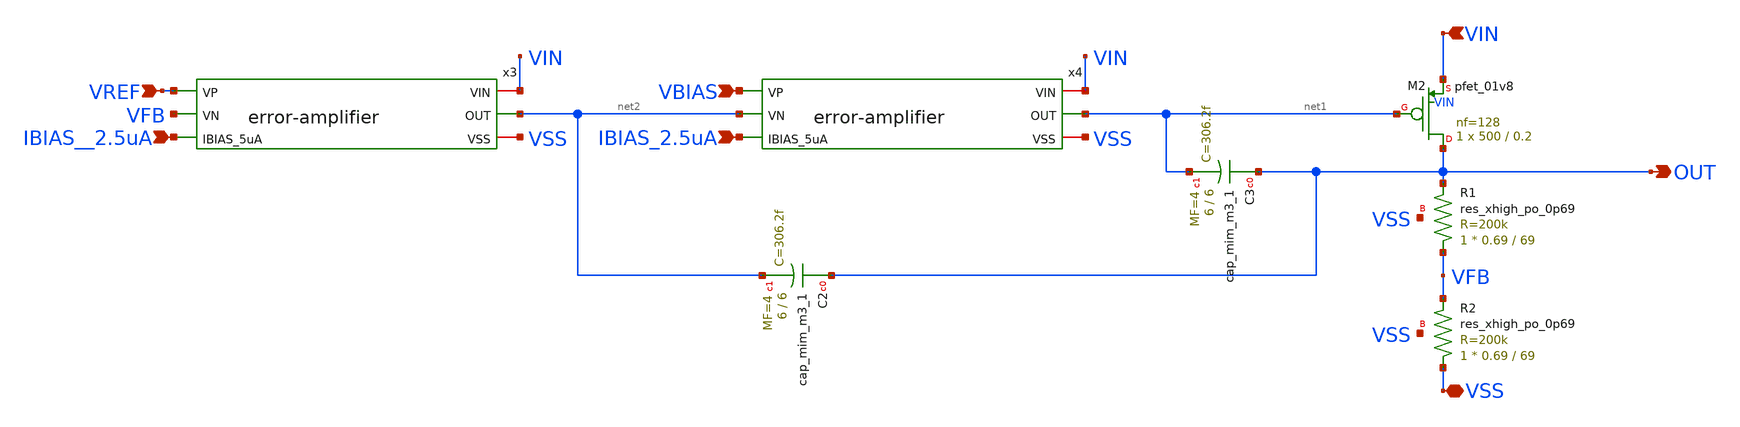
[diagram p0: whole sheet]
** sch_path: xschem/ldo_andriansyah/schematics/ldo-top.sch
**.subckt ldo-top VREF VIN IBIAS__2.5uA VSS IBIAS_2.5uA VBIAS OUT
*.ipin VREF
*.ipin VIN
*.ipin IBIAS__2.5uA
*.iopin VSS
*.ipin IBIAS_2.5uA
*.ipin VBIAS
*.opin OUT
XC2 OUT net2 sky130_fd_pr__cap_mim_m3_1 W=6 L=6 MF=4 m=4
XC3 OUT net1 sky130_fd_pr__cap_mim_m3_1 W=6 L=6 MF=4 m=4
x3 VIN VREF VFB IBIAS__2.5uA net2 VSS error-amplifier
XR1 VFB OUT VSS sky130_fd_pr__res_xhigh_po_0p69 L=69 mult=1 m=1
XR2 VSS VFB VSS sky130_fd_pr__res_xhigh_po_0p69 L=69 mult=1 m=1
XM2 OUT net1 VIN VIN sky130_fd_pr__pfet_01v8 L=0.2 W=500 nf=128 ad='int((nf+1)/2) * W/nf * 0.29' as='int((nf+2)/2) * W/nf * 0.29'
+ pd='2*int((nf+1)/2) * (W/nf + 0.29)' ps='2*int((nf+2)/2) * (W/nf + 0.29)' nrd='0.29 / W' nrs='0.29 / W'
+ sa=0 sb=0 sd=0 mult=1 m=1
x4 VIN VBIAS net2 IBIAS_2.5uA net1 VSS error-amplifier
**.ends

* expanding   symbol:
*+  /foss/designs/2026/tt_sky26b_ldo_andriansyah/xschem/error-amplifier/error-amplifier.sym # of pins=6
** sym_path: xschem/error-amplifier/error-amplifier.sym
** sch_path: xschem/error-amplifier/error-amplifier.sch
.subckt error-amplifier VIN VP VN IBIAS_5uA OUT VSS
*.ipin IBIAS_5uA
*.ipin VN
*.ipin VP
*.iopin VIN
*.iopin VSS
*.opin OUT
XM1 net2 net2 VSS VSS sky130_fd_pr__nfet_01v8 L=0.6 W=4.2 nf=4 ad='int((nf+1)/2) * W/nf * 0.29' as='int((nf+2)/2) * W/nf * 0.29'
+ pd='2*int((nf+1)/2) * (W/nf + 0.29)' ps='2*int((nf+2)/2) * (W/nf + 0.29)' nrd='0.29 / W' nrs='0.29 / W'
+ sa=0 sb=0 sd=0 mult=1 m=1
XM2 OUT net2 VSS VSS sky130_fd_pr__nfet_01v8 L=0.6 W=4.2 nf=4 ad='int((nf+1)/2) * W/nf * 0.29' as='int((nf+2)/2) * W/nf * 0.29'
+ pd='2*int((nf+1)/2) * (W/nf + 0.29)' ps='2*int((nf+2)/2) * (W/nf + 0.29)' nrd='0.29 / W' nrs='0.29 / W'
+ sa=0 sb=0 sd=0 mult=1 m=1
XM3 net2 VN net1 VDD sky130_fd_pr__pfet_01v8 L=0.6 W=28 nf=4 ad='int((nf+1)/2) * W/nf * 0.29' as='int((nf+2)/2) * W/nf * 0.29'
+ pd='2*int((nf+1)/2) * (W/nf + 0.29)' ps='2*int((nf+2)/2) * (W/nf + 0.29)' nrd='0.29 / W' nrs='0.29 / W'
+ sa=0 sb=0 sd=0 mult=1 m=1
XM4 OUT VP net1 VDD sky130_fd_pr__pfet_01v8 L=0.6 W=28 nf=4 ad='int((nf+1)/2) * W/nf * 0.29' as='int((nf+2)/2) * W/nf * 0.29'
+ pd='2*int((nf+1)/2) * (W/nf + 0.29)' ps='2*int((nf+2)/2) * (W/nf + 0.29)' nrd='0.29 / W' nrs='0.29 / W'
+ sa=0 sb=0 sd=0 mult=1 m=1
XM5 net1 IBIAS_5uA VIN VIN sky130_fd_pr__pfet_01v8 L=0.6 W=6.6 nf=4 ad='int((nf+1)/2) * W/nf * 0.29'
+ as='int((nf+2)/2) * W/nf * 0.29' pd='2*int((nf+1)/2) * (W/nf + 0.29)' ps='2*int((nf+2)/2) * (W/nf + 0.29)'
+ nrd='0.29 / W' nrs='0.29 / W' sa=0 sb=0 sd=0 mult=1 m=1
XM6 IBIAS_5uA IBIAS_5uA VIN VIN sky130_fd_pr__pfet_01v8 L=0.6 W=6.6 nf=4 ad='int((nf+1)/2) * W/nf * 0.29'
+ as='int((nf+2)/2) * W/nf * 0.29' pd='2*int((nf+1)/2) * (W/nf + 0.29)' ps='2*int((nf+2)/2) * (W/nf + 0.29)'
+ nrd='0.29 / W' nrs='0.29 / W' sa=0 sb=0 sd=0 mult=1 m=1
XM7 VDD VDD VDD VDD sky130_fd_pr__pfet_01v8 L=0.6 W=7 nf=1 ad='int((nf+1)/2) * W/nf * 0.29' as='int((nf+2)/2) * W/nf * 0.29'
+ pd='2*int((nf+1)/2) * (W/nf + 0.29)' ps='2*int((nf+2)/2) * (W/nf + 0.29)' nrd='0.29 / W' nrs='0.29 / W'
+ sa=0 sb=0 sd=0 mult=1 m=1
XM8 VSS VSS VSS VSS sky130_fd_pr__nfet_01v8 L=0.6 W=1.05 nf=1 ad='int((nf+1)/2) * W/nf * 0.29' as='int((nf+2)/2) * W/nf * 0.29'
+ pd='2*int((nf+1)/2) * (W/nf + 0.29)' ps='2*int((nf+2)/2) * (W/nf + 0.29)' nrd='0.29 / W' nrs='0.29 / W'
+ sa=0 sb=0 sd=0 mult=1 m=1
XM9 VDD VDD VDD VDD sky130_fd_pr__pfet_01v8 L=0.6 W=1.65 nf=1 ad='int((nf+1)/2) * W/nf * 0.29' as='int((nf+2)/2) * W/nf * 0.29'
+ pd='2*int((nf+1)/2) * (W/nf + 0.29)' ps='2*int((nf+2)/2) * (W/nf + 0.29)' nrd='0.29 / W' nrs='0.29 / W'
+ sa=0 sb=0 sd=0 mult=1 m=1
XM10 VSS VSS VSS VSS sky130_fd_pr__nfet_01v8 L=0.6 W=1.05 nf=1 ad='int((nf+1)/2) * W/nf * 0.29' as='int((nf+2)/2) * W/nf * 0.29'
+ pd='2*int((nf+1)/2) * (W/nf + 0.29)' ps='2*int((nf+2)/2) * (W/nf + 0.29)' nrd='0.29 / W' nrs='0.29 / W'
+ sa=0 sb=0 sd=0 mult=1 m=1
XM11 VDD VDD VDD VDD sky130_fd_pr__pfet_01v8 L=0.6 W=7 nf=1 ad='int((nf+1)/2) * W/nf * 0.29' as='int((nf+2)/2) * W/nf * 0.29'
+ pd='2*int((nf+1)/2) * (W/nf + 0.29)' ps='2*int((nf+2)/2) * (W/nf + 0.29)' nrd='0.29 / W' nrs='0.29 / W'
+ sa=0 sb=0 sd=0 mult=1 m=1
XM12 VDD VDD VDD VDD sky130_fd_pr__pfet_01v8 L=0.6 W=1.65 nf=1 ad='int((nf+1)/2) * W/nf * 0.29' as='int((nf+2)/2) * W/nf * 0.29'
+ pd='2*int((nf+1)/2) * (W/nf + 0.29)' ps='2*int((nf+2)/2) * (W/nf + 0.29)' nrd='0.29 / W' nrs='0.29 / W'
+ sa=0 sb=0 sd=0 mult=1 m=1
.ends

.end
